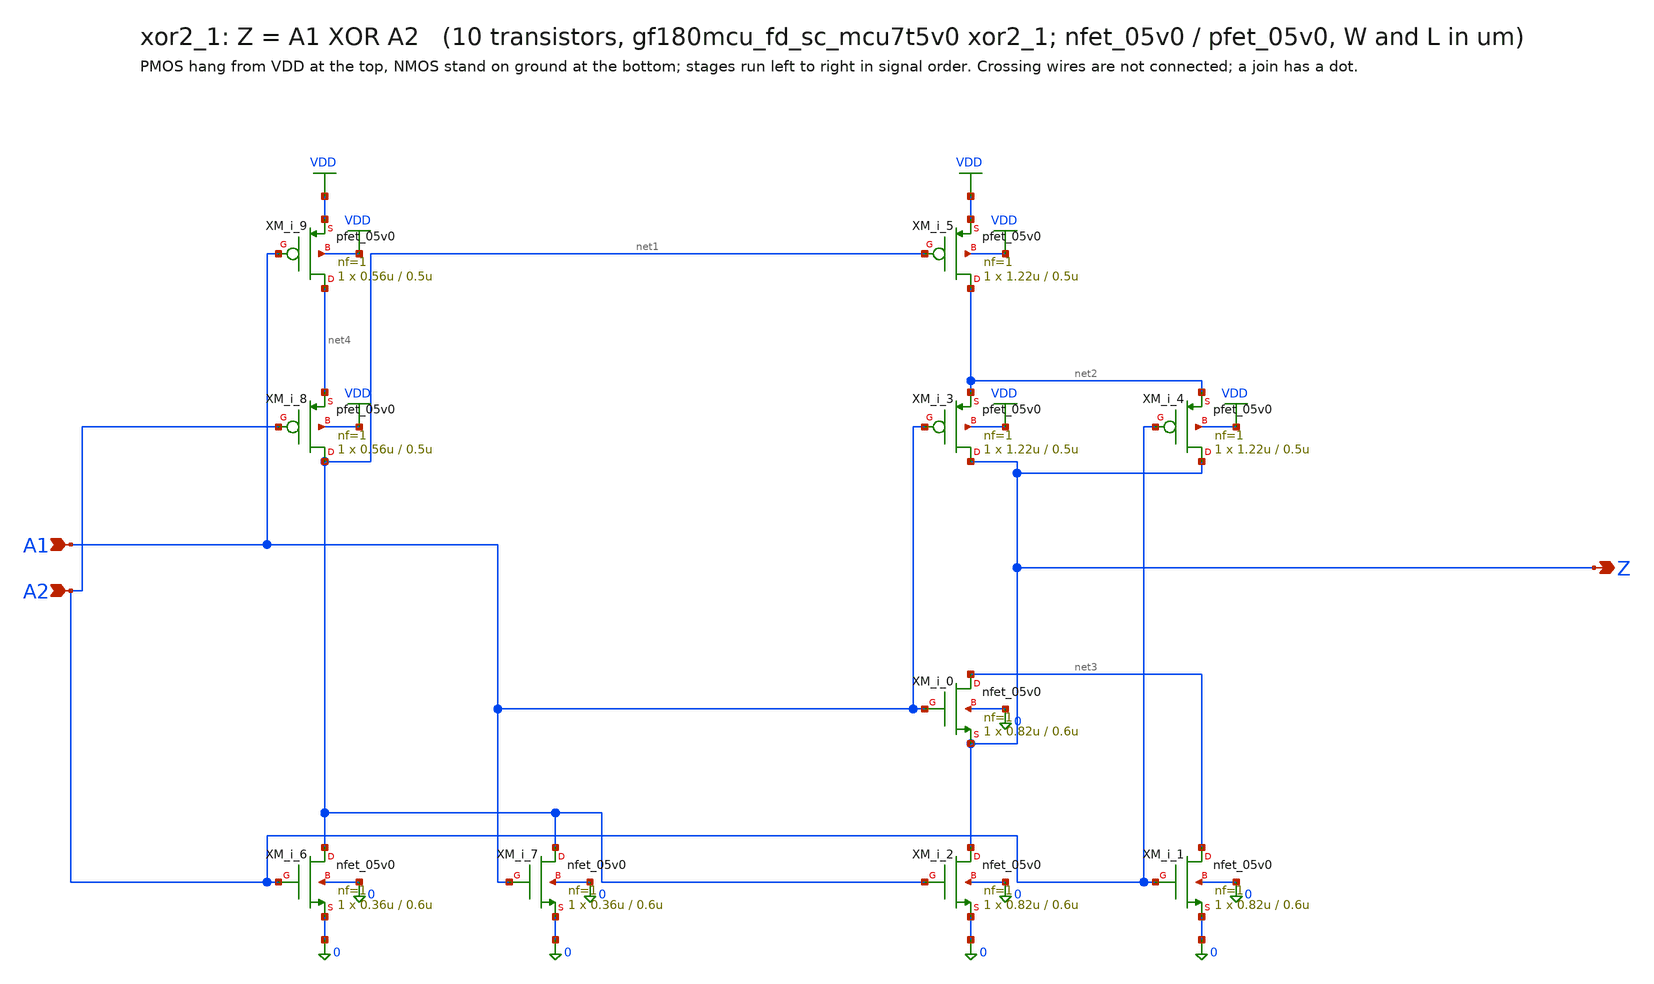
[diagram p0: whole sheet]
** sch_path: xschem/cells_tx/xor2_1.sch
**.subckt xor2_1 A1 A2 Z
*.ipin A1
*.ipin A2
*.opin Z
XM_i_6 net1 A2 0 0 nfet_05v0 L=0.6u W=0.36u nf=1 ad=1.8e-13 as=1.8e-13 pd=1.72e-06 ps=1.72e-06 nrd=0
+ nrs=0 sa=0 sb=0 sd=0 m=1
XM_i_7 net1 A1 0 0 nfet_05v0 L=0.6u W=0.36u nf=1 ad=1.8e-13 as=1.8e-13 pd=1.72e-06 ps=1.72e-06 nrd=0
+ nrs=0 sa=0 sb=0 sd=0 m=1
XM_i_2 Z net1 0 0 nfet_05v0 L=0.6u W=0.82u nf=1 ad=4.1e-13 as=4.1e-13 pd=2.64e-06 ps=2.64e-06 nrd=0
+ nrs=0 sa=0 sb=0 sd=0 m=1
XM_i_0 net3 A1 Z 0 nfet_05v0 L=0.6u W=0.82u nf=1 ad=4.1e-13 as=4.1e-13 pd=2.64e-06 ps=2.64e-06 nrd=0
+ nrs=0 sa=0 sb=0 sd=0 m=1
XM_i_1 net3 A2 0 0 nfet_05v0 L=0.6u W=0.82u nf=1 ad=4.1e-13 as=4.1e-13 pd=2.64e-06 ps=2.64e-06 nrd=0
+ nrs=0 sa=0 sb=0 sd=0 m=1
XM_i_8 net1 A2 net4 VDD pfet_05v0 L=0.5u W=0.56u nf=1 ad=2.8e-13 as=2.8e-13 pd=2.12e-06 ps=2.12e-06
+ nrd=0 nrs=0 sa=0 sb=0 sd=0 m=1
XM_i_9 net4 A1 VDD VDD pfet_05v0 L=0.5u W=0.56u nf=1 ad=2.8e-13 as=2.8e-13 pd=2.12e-06 ps=2.12e-06
+ nrd=0 nrs=0 sa=0 sb=0 sd=0 m=1
XM_i_5 net2 net1 VDD VDD pfet_05v0 L=0.5u W=1.22u nf=1 ad=6.1e-13 as=6.1e-13 pd=3.44e-06 ps=3.44e-06
+ nrd=0 nrs=0 sa=0 sb=0 sd=0 m=1
XM_i_3 Z A1 net2 VDD pfet_05v0 L=0.5u W=1.22u nf=1 ad=6.1e-13 as=6.1e-13 pd=3.44e-06 ps=3.44e-06
+ nrd=0 nrs=0 sa=0 sb=0 sd=0 m=1
XM_i_4 Z A2 net2 VDD pfet_05v0 L=0.5u W=1.22u nf=1 ad=6.1e-13 as=6.1e-13 pd=3.44e-06 ps=3.44e-06
+ nrd=0 nrs=0 sa=0 sb=0 sd=0 m=1
**.ends
.GLOBAL VDD
.end
